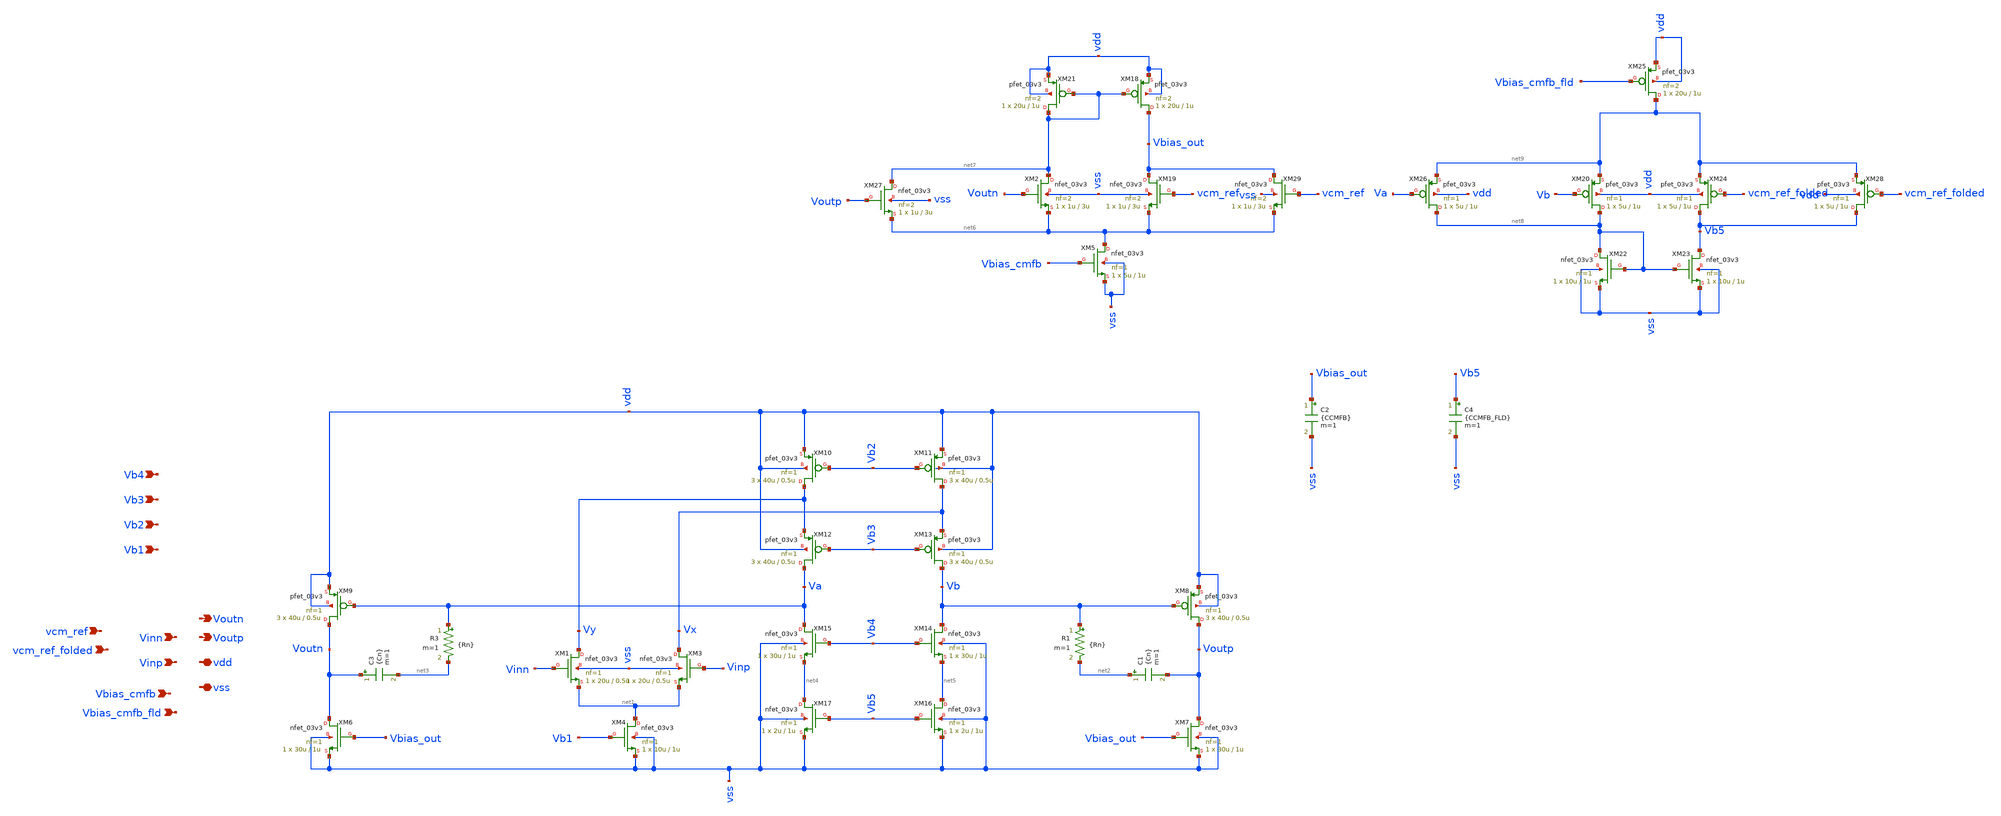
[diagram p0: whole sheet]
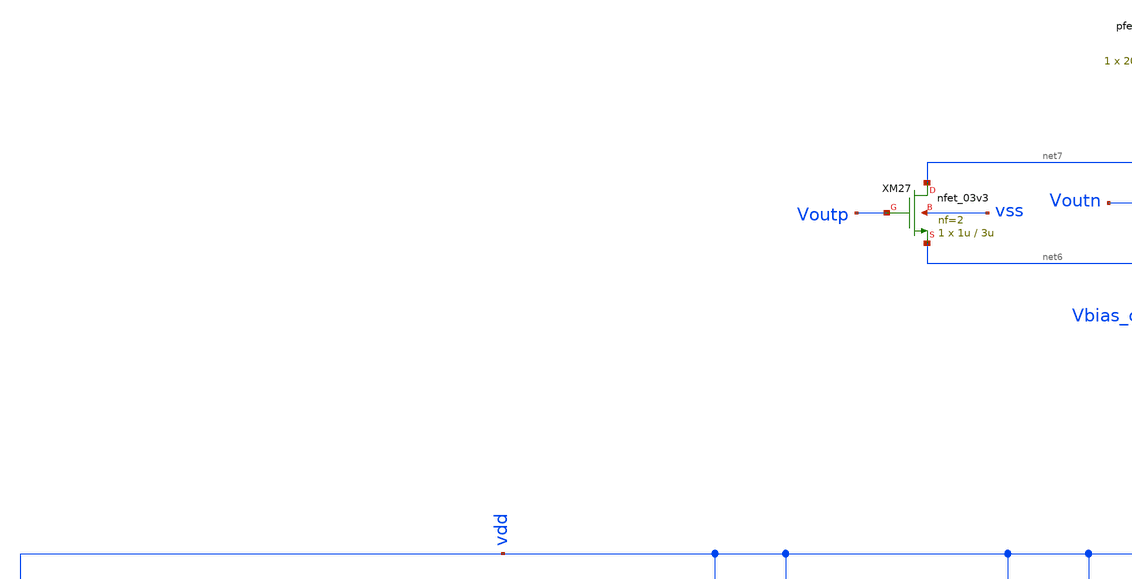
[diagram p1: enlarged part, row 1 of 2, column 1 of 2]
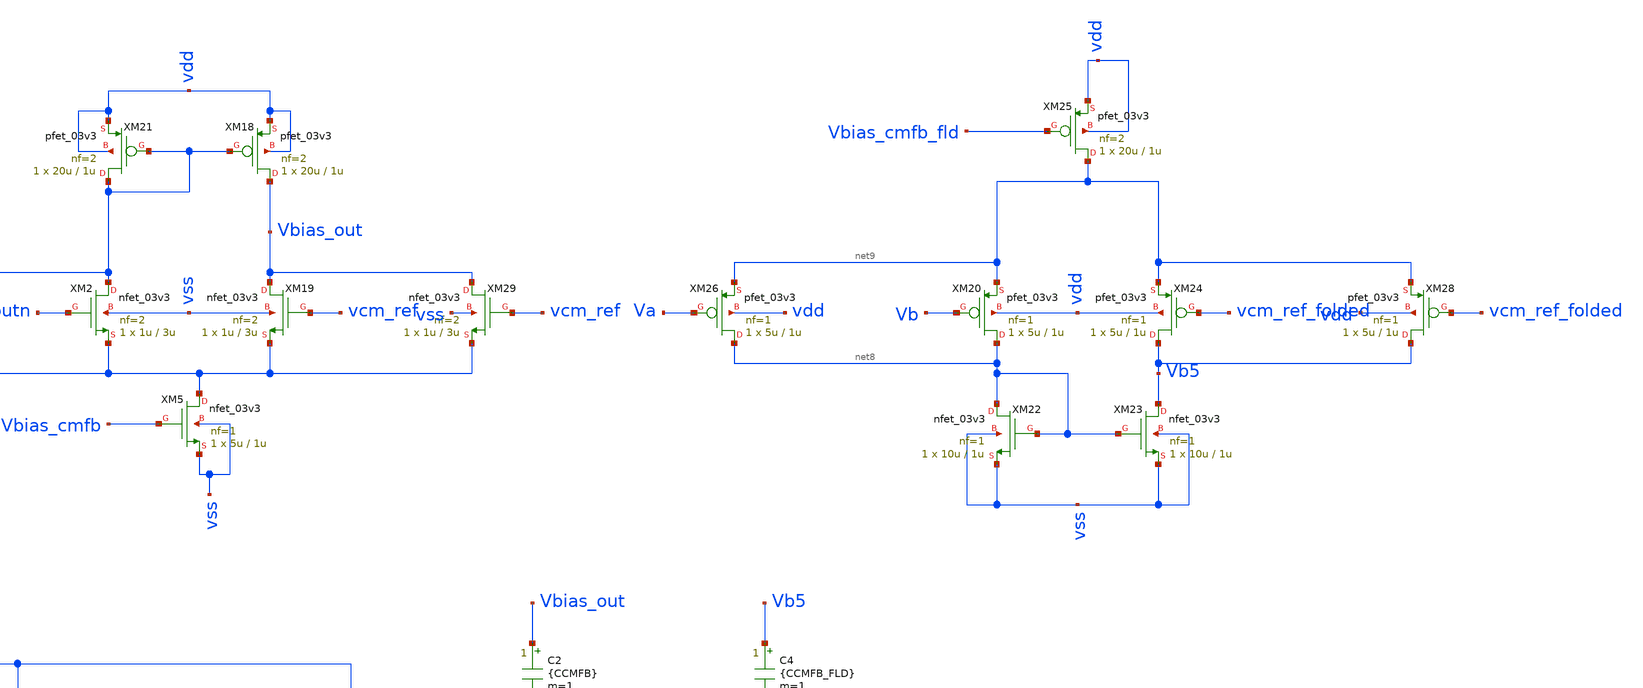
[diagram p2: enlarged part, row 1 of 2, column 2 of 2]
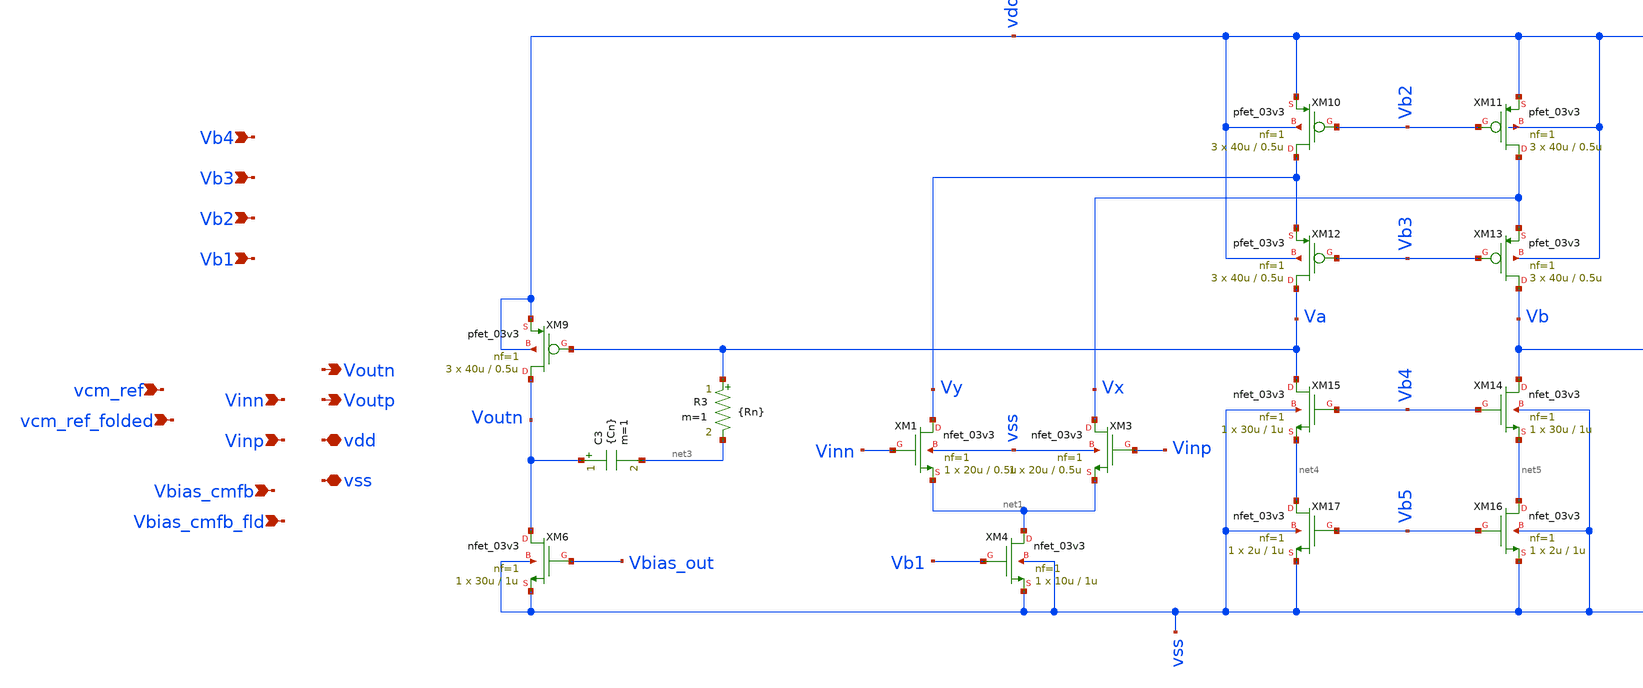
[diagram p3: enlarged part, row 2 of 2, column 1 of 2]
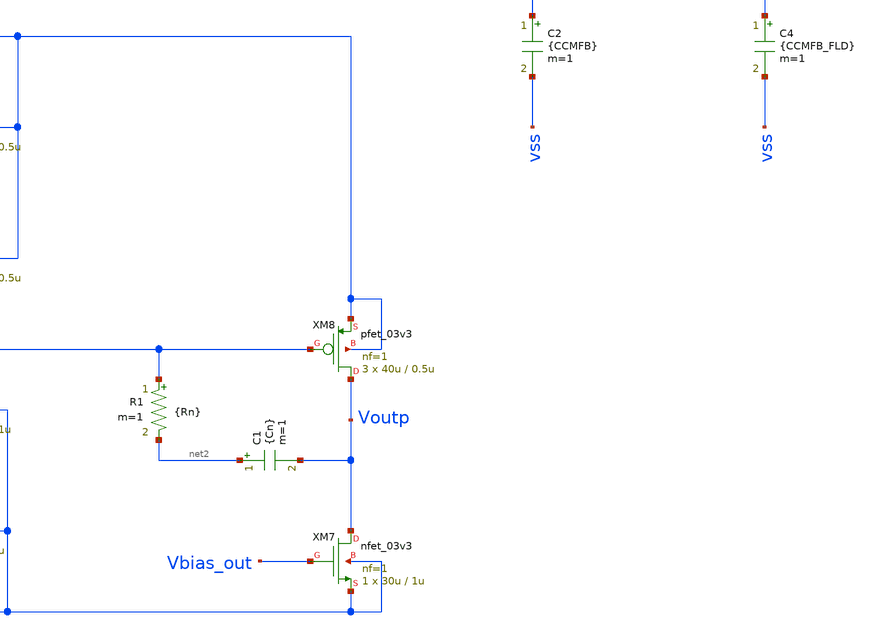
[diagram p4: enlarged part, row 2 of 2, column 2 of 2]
** sch_path: circuit_files/sar_adc_test/xschem/op-amp_diff.sch
**.subckt op-amp_diff Vinn Voutp vdd Vinp Vb1 Vbias_cmfb_fld vss Voutn Vbias_cmfb Vb2 Vb3 Vb4
*+ vcm_ref_folded vcm_ref
*.ipin Vinn
*.opin Voutp
*.iopin vdd
*.ipin Vinp
*.ipin Vb1
*.ipin Vbias_cmfb_fld
*.iopin vss
*.opin Voutn
*.ipin Vbias_cmfb
*.ipin Vb2
*.ipin Vb3
*.ipin Vb4
*.ipin vcm_ref_folded
*.ipin vcm_ref
XM1 Vy Vinn net1 vss nfet_03v3 L=0.5u W=20u nf=1 ad='int((nf+1)/2) * W/nf * 0.18u' as='int((nf+2)/2) * W/nf * 0.18u'
+ pd='2*int((nf+1)/2) * (W/nf + 0.18u)' ps='2*int((nf+2)/2) * (W/nf + 0.18u)' nrd='0.18u / W' nrs='0.18u / W'
+ sa=0 sb=0 sd=0 m=1
XM4 net1 Vb1 vss vss nfet_03v3 L=1u W=10u nf=1 ad='int((nf+1)/2) * W/nf * 0.18u' as='int((nf+2)/2) * W/nf * 0.18u'
+ pd='2*int((nf+1)/2) * (W/nf + 0.18u)' ps='2*int((nf+2)/2) * (W/nf + 0.18u)' nrd='0.18u / W' nrs='0.18u / W'
+ sa=0 sb=0 sd=0 m=1
XM3 Vx Vinp net1 vss nfet_03v3 L=0.5u W=20u nf=1 ad='int((nf+1)/2) * W/nf * 0.18u' as='int((nf+2)/2) * W/nf * 0.18u'
+ pd='2*int((nf+1)/2) * (W/nf + 0.18u)' ps='2*int((nf+2)/2) * (W/nf + 0.18u)' nrd='0.18u / W' nrs='0.18u / W'
+ sa=0 sb=0 sd=0 m=1
XM7 Voutp Vbias_out vss vss nfet_03v3 L=1u W=30u nf=1 ad='int((nf+1)/2) * W/nf * 0.18u' as='int((nf+2)/2) * W/nf * 0.18u'
+ pd='2*int((nf+1)/2) * (W/nf + 0.18u)' ps='2*int((nf+2)/2) * (W/nf + 0.18u)' nrd='0.18u / W' nrs='0.18u / W'
+ sa=0 sb=0 sd=0 m=1
XM8 Voutp Vb vdd vdd pfet_03v3 L=0.5u W=40u nf=1 ad='int((nf+1)/2) * W/nf * 0.18u' as='int((nf+2)/2) * W/nf * 0.18u'
+ pd='2*int((nf+1)/2) * (W/nf + 0.18u)' ps='2*int((nf+2)/2) * (W/nf + 0.18u)' nrd='0.18u / W' nrs='0.18u / W'
+ sa=0 sb=0 sd=0 m=3
XM6 Voutn Vbias_out vss vss nfet_03v3 L=1u W=30u nf=1 ad='int((nf+1)/2) * W/nf * 0.18u' as='int((nf+2)/2) * W/nf * 0.18u'
+ pd='2*int((nf+1)/2) * (W/nf + 0.18u)' ps='2*int((nf+2)/2) * (W/nf + 0.18u)' nrd='0.18u / W' nrs='0.18u / W'
+ sa=0 sb=0 sd=0 m=1
XM9 Voutn Va vdd vdd pfet_03v3 L=0.5u W=40u nf=1 ad='int((nf+1)/2) * W/nf * 0.18u' as='int((nf+2)/2) * W/nf * 0.18u'
+ pd='2*int((nf+1)/2) * (W/nf + 0.18u)' ps='2*int((nf+2)/2) * (W/nf + 0.18u)' nrd='0.18u / W' nrs='0.18u / W'
+ sa=0 sb=0 sd=0 m=3
XM10 Vy Vb2 vdd vdd pfet_03v3 L=0.5u W=40u nf=1 ad='int((nf+1)/2) * W/nf * 0.18u' as='int((nf+2)/2) * W/nf * 0.18u'
+ pd='2*int((nf+1)/2) * (W/nf + 0.18u)' ps='2*int((nf+2)/2) * (W/nf + 0.18u)' nrd='0.18u / W' nrs='0.18u / W'
+ sa=0 sb=0 sd=0 m=3
XM11 Vx Vb2 vdd vdd pfet_03v3 L=0.5u W=40u nf=1 ad='int((nf+1)/2) * W/nf * 0.18u' as='int((nf+2)/2) * W/nf * 0.18u'
+ pd='2*int((nf+1)/2) * (W/nf + 0.18u)' ps='2*int((nf+2)/2) * (W/nf + 0.18u)' nrd='0.18u / W' nrs='0.18u / W'
+ sa=0 sb=0 sd=0 m=3
XM12 Va Vb3 Vy vdd pfet_03v3 L=0.5u W=40u nf=1 ad='int((nf+1)/2) * W/nf * 0.18u' as='int((nf+2)/2) * W/nf * 0.18u'
+ pd='2*int((nf+1)/2) * (W/nf + 0.18u)' ps='2*int((nf+2)/2) * (W/nf + 0.18u)' nrd='0.18u / W' nrs='0.18u / W'
+ sa=0 sb=0 sd=0 m=3
XM13 Vb Vb3 Vx vdd pfet_03v3 L=0.5u W=40u nf=1 ad='int((nf+1)/2) * W/nf * 0.18u' as='int((nf+2)/2) * W/nf * 0.18u'
+ pd='2*int((nf+1)/2) * (W/nf + 0.18u)' ps='2*int((nf+2)/2) * (W/nf + 0.18u)' nrd='0.18u / W' nrs='0.18u / W'
+ sa=0 sb=0 sd=0 m=3
XM14 Vb Vb4 net5 vss nfet_03v3 L=1u W=30u nf=1 ad='int((nf+1)/2) * W/nf * 0.18u' as='int((nf+2)/2) * W/nf * 0.18u'
+ pd='2*int((nf+1)/2) * (W/nf + 0.18u)' ps='2*int((nf+2)/2) * (W/nf + 0.18u)' nrd='0.18u / W' nrs='0.18u / W'
+ sa=0 sb=0 sd=0 m=1
XM15 Va Vb4 net4 vss nfet_03v3 L=1u W=30u nf=1 ad='int((nf+1)/2) * W/nf * 0.18u' as='int((nf+2)/2) * W/nf * 0.18u'
+ pd='2*int((nf+1)/2) * (W/nf + 0.18u)' ps='2*int((nf+2)/2) * (W/nf + 0.18u)' nrd='0.18u / W' nrs='0.18u / W'
+ sa=0 sb=0 sd=0 m=1
XM16 net5 Vb5 vss vss nfet_03v3 L=1u W=2u nf=1 ad='int((nf+1)/2) * W/nf * 0.18u' as='int((nf+2)/2) * W/nf * 0.18u'
+ pd='2*int((nf+1)/2) * (W/nf + 0.18u)' ps='2*int((nf+2)/2) * (W/nf + 0.18u)' nrd='0.18u / W' nrs='0.18u / W'
+ sa=0 sb=0 sd=0 m=1
XM17 net4 Vb5 vss vss nfet_03v3 L=1u W=2u nf=1 ad='int((nf+1)/2) * W/nf * 0.18u' as='int((nf+2)/2) * W/nf * 0.18u'
+ pd='2*int((nf+1)/2) * (W/nf + 0.18u)' ps='2*int((nf+2)/2) * (W/nf + 0.18u)' nrd='0.18u / W' nrs='0.18u / W'
+ sa=0 sb=0 sd=0 m=1
C3 Voutn net3 {Cn} m=1
R3 Va net3 {Rn} m=1
R1 Vb net2 {Rn} m=1
C1 net2 Voutp {Cn} m=1
C2 Vbias_out vss {CCMFB} m=1
XM2 net7 Voutn net6 vss nfet_03v3 L=3u W=1u nf=2 ad='int((nf+1)/2) * W/nf * 0.18u' as='int((nf+2)/2) * W/nf * 0.18u'
+ pd='2*int((nf+1)/2) * (W/nf + 0.18u)' ps='2*int((nf+2)/2) * (W/nf + 0.18u)' nrd='0.18u / W' nrs='0.18u / W'
+ sa=0 sb=0 sd=0 m=1
XM5 net6 Vbias_cmfb vss vss nfet_03v3 L=1u W=5u nf=1 ad='int((nf+1)/2) * W/nf * 0.18u' as='int((nf+2)/2) * W/nf * 0.18u'
+ pd='2*int((nf+1)/2) * (W/nf + 0.18u)' ps='2*int((nf+2)/2) * (W/nf + 0.18u)' nrd='0.18u / W' nrs='0.18u / W'
+ sa=0 sb=0 sd=0 m=1
XM18 Vbias_out net7 vdd vdd pfet_03v3 L=1u W=20u nf=2 ad='int((nf+1)/2) * W/nf * 0.18u' as='int((nf+2)/2) * W/nf * 0.18u'
+ pd='2*int((nf+1)/2) * (W/nf + 0.18u)' ps='2*int((nf+2)/2) * (W/nf + 0.18u)' nrd='0.18u / W' nrs='0.18u / W'
+ sa=0 sb=0 sd=0 m=1
XM19 Vbias_out vcm_ref net6 vss nfet_03v3 L=3u W=1u nf=2 ad='int((nf+1)/2) * W/nf * 0.18u' as='int((nf+2)/2) * W/nf * 0.18u'
+ pd='2*int((nf+1)/2) * (W/nf + 0.18u)' ps='2*int((nf+2)/2) * (W/nf + 0.18u)' nrd='0.18u / W' nrs='0.18u / W'
+ sa=0 sb=0 sd=0 m=1
XM21 net7 net7 vdd vdd pfet_03v3 L=1u W=20u nf=2 ad='int((nf+1)/2) * W/nf * 0.18u' as='int((nf+2)/2) * W/nf * 0.18u'
+ pd='2*int((nf+1)/2) * (W/nf + 0.18u)' ps='2*int((nf+2)/2) * (W/nf + 0.18u)' nrd='0.18u / W' nrs='0.18u / W'
+ sa=0 sb=0 sd=0 m=1
C4 Vb5 vss {CCMFB_FLD} m=1
XM20 net8 Vb net9 vdd pfet_03v3 L=1u W=5u nf=1 ad='int((nf+1)/2) * W/nf * 0.18u' as='int((nf+2)/2) * W/nf * 0.18u'
+ pd='2*int((nf+1)/2) * (W/nf + 0.18u)' ps='2*int((nf+2)/2) * (W/nf + 0.18u)' nrd='0.18u / W' nrs='0.18u / W'
+ sa=0 sb=0 sd=0 m=1
XM24 Vb5 vcm_ref_folded net9 vdd pfet_03v3 L=1u W=5u nf=1 ad='int((nf+1)/2) * W/nf * 0.18u' as='int((nf+2)/2) * W/nf * 0.18u'
+ pd='2*int((nf+1)/2) * (W/nf + 0.18u)' ps='2*int((nf+2)/2) * (W/nf + 0.18u)' nrd='0.18u / W' nrs='0.18u / W'
+ sa=0 sb=0 sd=0 m=1
XM22 net8 net8 vss vss nfet_03v3 L=1u W=10u nf=1 ad='int((nf+1)/2) * W/nf * 0.18u' as='int((nf+2)/2) * W/nf * 0.18u'
+ pd='2*int((nf+1)/2) * (W/nf + 0.18u)' ps='2*int((nf+2)/2) * (W/nf + 0.18u)' nrd='0.18u / W' nrs='0.18u / W'
+ sa=0 sb=0 sd=0 m=1
XM23 Vb5 net8 vss vss nfet_03v3 L=1u W=10u nf=1 ad='int((nf+1)/2) * W/nf * 0.18u' as='int((nf+2)/2) * W/nf * 0.18u'
+ pd='2*int((nf+1)/2) * (W/nf + 0.18u)' ps='2*int((nf+2)/2) * (W/nf + 0.18u)' nrd='0.18u / W' nrs='0.18u / W'
+ sa=0 sb=0 sd=0 m=1
XM25 net9 Vbias_cmfb_fld vdd vdd pfet_03v3 L=1u W=20u nf=2 ad='int((nf+1)/2) * W/nf * 0.18u' as='int((nf+2)/2) * W/nf * 0.18u'
+ pd='2*int((nf+1)/2) * (W/nf + 0.18u)' ps='2*int((nf+2)/2) * (W/nf + 0.18u)' nrd='0.18u / W' nrs='0.18u / W'
+ sa=0 sb=0 sd=0 m=1
XM26 net8 Va net9 vdd pfet_03v3 L=1u W=5u nf=1 ad='int((nf+1)/2) * W/nf * 0.18u' as='int((nf+2)/2) * W/nf * 0.18u'
+ pd='2*int((nf+1)/2) * (W/nf + 0.18u)' ps='2*int((nf+2)/2) * (W/nf + 0.18u)' nrd='0.18u / W' nrs='0.18u / W'
+ sa=0 sb=0 sd=0 m=1
XM28 Vb5 vcm_ref_folded net9 vdd pfet_03v3 L=1u W=5u nf=1 ad='int((nf+1)/2) * W/nf * 0.18u' as='int((nf+2)/2) * W/nf * 0.18u'
+ pd='2*int((nf+1)/2) * (W/nf + 0.18u)' ps='2*int((nf+2)/2) * (W/nf + 0.18u)' nrd='0.18u / W' nrs='0.18u / W'
+ sa=0 sb=0 sd=0 m=1
XM27 net7 Voutp net6 vss nfet_03v3 L=3u W=1u nf=2 ad='int((nf+1)/2) * W/nf * 0.18u' as='int((nf+2)/2) * W/nf * 0.18u'
+ pd='2*int((nf+1)/2) * (W/nf + 0.18u)' ps='2*int((nf+2)/2) * (W/nf + 0.18u)' nrd='0.18u / W' nrs='0.18u / W'
+ sa=0 sb=0 sd=0 m=1
XM29 Vbias_out vcm_ref net6 vss nfet_03v3 L=3u W=1u nf=2 ad='int((nf+1)/2) * W/nf * 0.18u' as='int((nf+2)/2) * W/nf * 0.18u'
+ pd='2*int((nf+1)/2) * (W/nf + 0.18u)' ps='2*int((nf+2)/2) * (W/nf + 0.18u)' nrd='0.18u / W' nrs='0.18u / W'
+ sa=0 sb=0 sd=0 m=1
**.ends
.end
